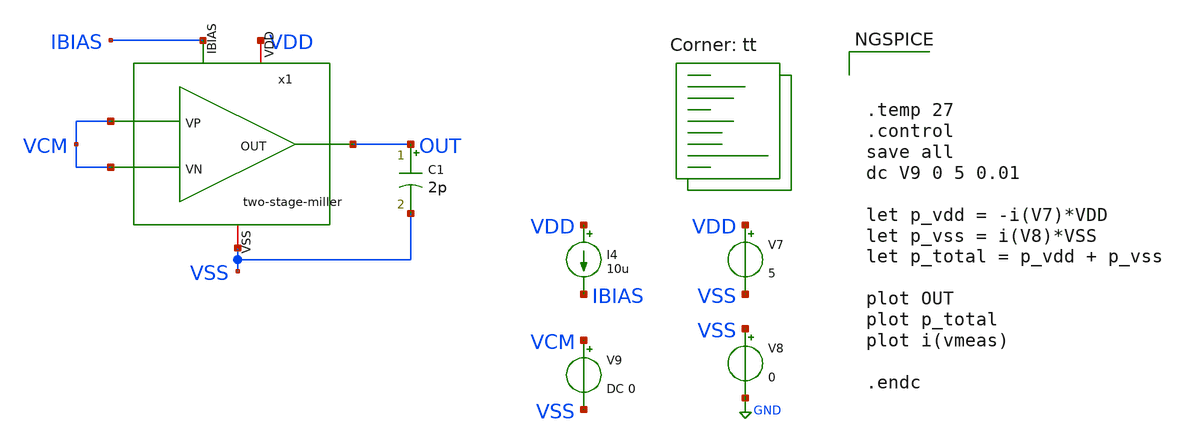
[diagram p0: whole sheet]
** sch_path: xschem/error-amplifier/testbench/untitled-2.sch
**.subckt untitled-2
V7 VDD VSS 5
V8 VSS GND 0
I4 VDD IBIAS 10u
C1 OUT VSS 2p m=1
V9 VCM VSS DC 0
x1 VDD OUT VCM VCM IBIAS VSS two-stage-miller
**** begin user architecture code



.temp 27
.control
save all
dc V9 0 5 0.01

let p_vdd = -i(V7)*VDD
let p_vss = i(V8)*VSS
let p_total = p_vdd + p_vss

plot OUT
plot p_total
plot i(vmeas)

.endc


.lib $::SKYWATER_MODELS/sky130.lib.spice tt
**** end user architecture code
**.ends

* expanding   symbol:  icdec-biomedical-pmic/xschem/error-amplifier/schematics/two-stage-miller.sym
*+ # of pins=6
** sym_path: xschem/error-amplifier/schematics/two-stage-miller.sym
** sch_path: xschem/error-amplifier/schematics/two-stage-miller.sch
.subckt two-stage-miller VDD OUT VP VN IBIAS VSS
*.iopin VDD
*.iopin VSS
*.ipin IBIAS
*.ipin VP
*.ipin VN
*.opin OUT
XM1 net3 net2 VDD VDD sky130_fd_pr__pfet_g5v0d10v5 L=1.25 W=75.2 nf=8 ad='int((nf+1)/2) * W/nf * 0.29'
+ as='int((nf+2)/2) * W/nf * 0.29' pd='2*int((nf+1)/2) * (W/nf + 0.29)' ps='2*int((nf+2)/2) * (W/nf + 0.29)'
+ nrd='0.29 / W' nrs='0.29 / W' sa=0 sb=0 sd=0 mult=1 m=1
XM2 net2 net2 VDD VDD sky130_fd_pr__pfet_g5v0d10v5 L=1.25 W=75.2 nf=8 ad='int((nf+1)/2) * W/nf * 0.29'
+ as='int((nf+2)/2) * W/nf * 0.29' pd='2*int((nf+1)/2) * (W/nf + 0.29)' ps='2*int((nf+2)/2) * (W/nf + 0.29)'
+ nrd='0.29 / W' nrs='0.29 / W' sa=0 sb=0 sd=0 mult=1 m=1
XM3 net3 VN net1 VSS sky130_fd_pr__nfet_g5v0d10v5 L=0.5 W=37.7 nf=8 ad='int((nf+1)/2) * W/nf * 0.29'
+ as='int((nf+2)/2) * W/nf * 0.29' pd='2*int((nf+1)/2) * (W/nf + 0.29)' ps='2*int((nf+2)/2) * (W/nf + 0.29)'
+ nrd='0.29 / W' nrs='0.29 / W' sa=0 sb=0 sd=0 mult=1 m=1
XM4 net2 VP net1 VSS sky130_fd_pr__nfet_g5v0d10v5 L=0.5 W=37.7 nf=8 ad='int((nf+1)/2) * W/nf * 0.29'
+ as='int((nf+2)/2) * W/nf * 0.29' pd='2*int((nf+1)/2) * (W/nf + 0.29)' ps='2*int((nf+2)/2) * (W/nf + 0.29)'
+ nrd='0.29 / W' nrs='0.29 / W' sa=0 sb=0 sd=0 mult=1 m=1
XM5 net1 IBIAS VSS VSS sky130_fd_pr__nfet_g5v0d10v5 L=1.25 W=60 nf=8 ad='int((nf+1)/2) * W/nf * 0.29'
+ as='int((nf+2)/2) * W/nf * 0.29' pd='2*int((nf+1)/2) * (W/nf + 0.29)' ps='2*int((nf+2)/2) * (W/nf + 0.29)'
+ nrd='0.29 / W' nrs='0.29 / W' sa=0 sb=0 sd=0 mult=1 m=1
XM6 IBIAS IBIAS VSS VSS sky130_fd_pr__nfet_g5v0d10v5 L=1.25 W=60 nf=8 ad='int((nf+1)/2) * W/nf * 0.29'
+ as='int((nf+2)/2) * W/nf * 0.29' pd='2*int((nf+1)/2) * (W/nf + 0.29)' ps='2*int((nf+2)/2) * (W/nf + 0.29)'
+ nrd='0.29 / W' nrs='0.29 / W' sa=0 sb=0 sd=0 mult=1 m=1
XM7 OUT net3 VDD VDD sky130_fd_pr__pfet_g5v0d10v5 L=1.25 W=160 nf=16 ad='int((nf+1)/2) * W/nf * 0.29'
+ as='int((nf+2)/2) * W/nf * 0.29' pd='2*int((nf+1)/2) * (W/nf + 0.29)' ps='2*int((nf+2)/2) * (W/nf + 0.29)'
+ nrd='0.29 / W' nrs='0.29 / W' sa=0 sb=0 sd=0 mult=1 m=1
XM8 OUT IBIAS VSS VSS sky130_fd_pr__nfet_g5v0d10v5 L=1.25 W=60 nf=8 ad='int((nf+1)/2) * W/nf * 0.29'
+ as='int((nf+2)/2) * W/nf * 0.29' pd='2*int((nf+1)/2) * (W/nf + 0.29)' ps='2*int((nf+2)/2) * (W/nf + 0.29)'
+ nrd='0.29 / W' nrs='0.29 / W' sa=0 sb=0 sd=0 mult=1 m=1
XC1 net4 net3 sky130_fd_pr__cap_mim_m3_1 W=25 L=25 MF=8 m=8
XM9 OUT VSS net4 VDD sky130_fd_pr__pfet_g5v0d10v5 L=0.9 W=20 nf=4 ad='int((nf+1)/2) * W/nf * 0.29' as='int((nf+2)/2) * W/nf * 0.29'
+ pd='2*int((nf+1)/2) * (W/nf + 0.29)' ps='2*int((nf+2)/2) * (W/nf + 0.29)' nrd='0.29 / W' nrs='0.29 / W'
+ sa=0 sb=0 sd=0 mult=1 m=1
.ends

.GLOBAL GND
.end
